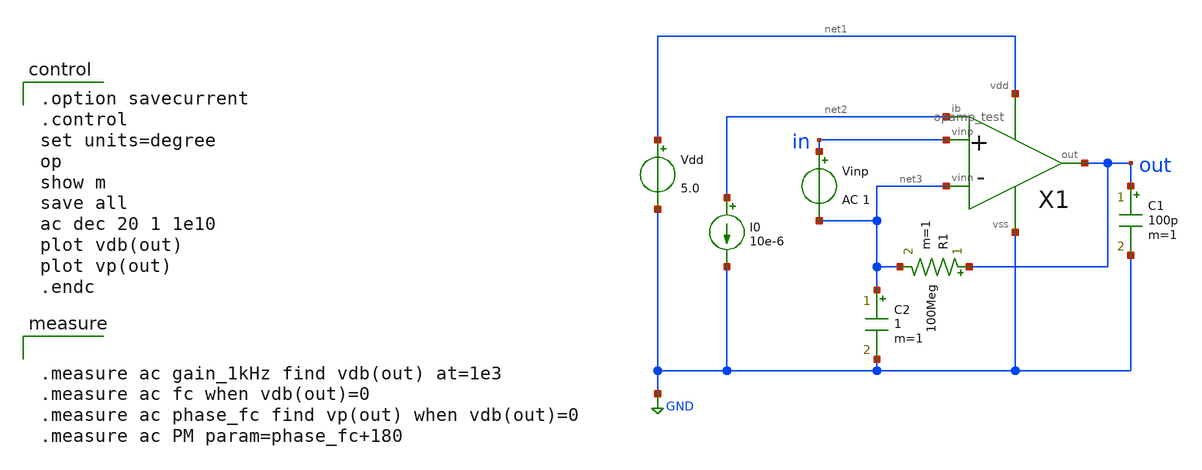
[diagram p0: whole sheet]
** sch_path: member_project/opamp/cat_nekonekone/opamp_ac.sch
**.subckt opamp_ac
Vdd net1 GND 5.0
Vinp in net3 AC 1
C1 out GND 100p m=1
I0 net2 GND 10e-6
R1 out net3 100Meg m=1
C2 net3 GND 1 m=1
X1 in net3 net2 out net1 GND opamp_test
**** begin user architecture code

.option savecurrent
.control
set units=degree
op
show m
save all
ac dec 20 1 1e10
plot vdb(out)
plot vp(out)
.endc



.measure ac gain_1kHz find vdb(out) at=1e3
.measure ac fc when vdb(out)=0
.measure ac phase_fc find vp(out) when vdb(out)=0
.measure ac PM param=phase_fc+180

 .include $::LIB/ip62_models
**** end user architecture code
**.ends

* expanding   symbol:  opamp_test.sym # of pins=6
** sym_path: member_project/opamp/cat_nekonekone/opamp_test.sym
** sch_path: member_project/opamp/cat_nekonekone/opamp_test.sch
.subckt opamp_test vinp vinn ib out vdd vss
*.ipin vinn
*.ipin vinp
*.opin out
*.iopin ib
*.iopin vss
*.iopin vdd
XXM1 net2 vinn net1 vdd PMOS w=25u l=5u nrd=0 nrs=0 m=12
XXM4 net3 net2 vss vss NMOS w=25u l=5u nrd=0 nrs=0 m=8
XXM2 net3 vinp net1 vdd PMOS w=25u l=5u nrd=0 nrs=0 m=12
XXM3 net2 net2 vss vss NMOS w=25u l=5u nrd=0 nrs=0 m=8
XXM5 net1 ib vdd vdd PMOS w=25u l=5u nrd=0 nrs=0 m=16
XXM6 out ib vdd vdd PMOS w=25u l=5u nrd=0 nrs=0 m=32
XXM7 out net3 vss vss NMOS w=25u l=5u nrd=0 nrs=0 m=34
XXM8 ib ib vdd vdd PMOS w=25u l=5u nrd=0 nrs=0 m=1
XXM9 net5 ib vdd vdd PMOS w=25u l=5u nrd=0 nrs=0 m=2
XXM10 net5 net5 net4 vss NMOS w=25u l=5u nrd=0 nrs=0 m=2
XXM11 net4 net4 vss vss NMOS w=25u l=5u nrd=0 nrs=0 m=2
XXM12 net6 net5 net3 vss NMOS w=25u l=5u nrd=0 nrs=0 m=4
XXM_DUMMY2 vdd vdd vdd vdd PMOS w=25u l=5u nrd=0 nrs=0 m=4
XXM_DUMMY1 vss vss vss vss NMOS w=25u l=5u nrd=0 nrs=0 m=24
XXM_DUMMY3 net1 vdd vdd vdd PMOS w=25u l=5u nrd=0 nrs=0 m=4
XXM_DUMMY5 net3 vss vss vss NMOS w=25u l=5u nrd=0 nrs=0 m=2
XXM_DUMMY4 net5 vdd vdd vdd PMOS w=25u l=5u nrd=0 nrs=0 m=2
XXM_DUMMY6 ib vdd vdd vdd PMOS w=25u l=5u nrd=0 nrs=0 m=1
XXM_DUMMY7 out vss vss vss NMOS w=25u l=5u nrd=0 nrs=0 m=2
XXC2 net6 out vss F_CSIO c=4.954p x=96u y=86u m=4
.ends

.GLOBAL GND
.end
